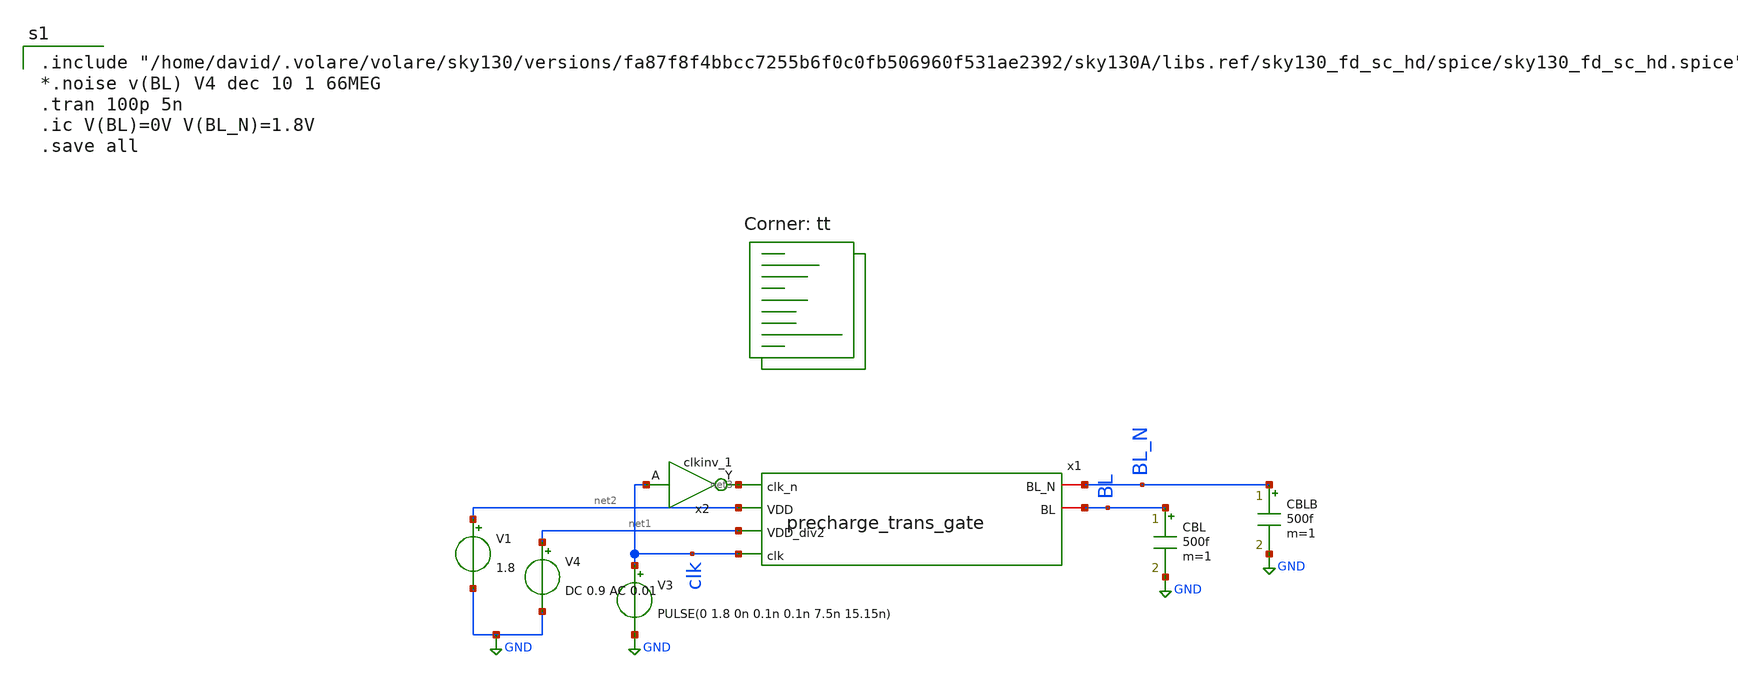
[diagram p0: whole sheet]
** sch_path: analog/schematics/trans_gate_tb.sch
**.subckt trans_gate_tb
V3 clk GND PULSE(0 1.8 0n 0.1n 0.1n 7.5n 15.15n)
x2 clk VGND VNB VPB VPWR net3 sky130_fd_sc_hd__clkinv_1
V4 net1 GND DC 0.9 AC 0.01
CBLB BL_N GND 500f m=1
CBL BL GND 500f m=1
x1 net3 BL_N BL net2 net1 clk precharge_trans_gate
V1 net2 GND 1.8
**** begin user architecture code

.include "/home/david/.volare/volare/sky130/versions/fa87f8f4bbcc7255b6f0c0fb506960f531ae2392/sky130A/libs.ref/sky130_fd_sc_hd/spice/sky130_fd_sc_hd.spice"
*.noise v(BL) V4 dec 10 1 66MEG
.tran 100p 5n
.ic V(BL)=0V V(BL_N)=1.8V
.save all

.lib $::SKYWATER_MODELS/sky130.lib.spice tt
**** end user architecture code
**.ends
.GLOBAL GND
.end
